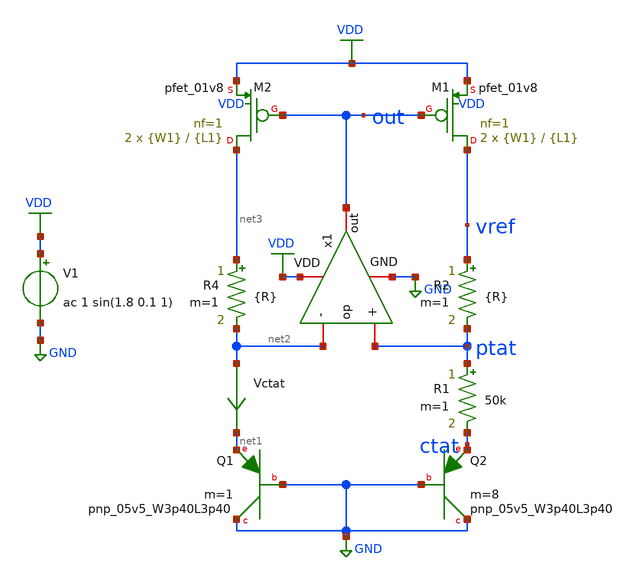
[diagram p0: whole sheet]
** sch_path: xschem/bgr_op3.sch
**.subckt bgr_op3
XQ1 GND GND net1 sky130_fd_pr__pnp_05v5_W3p40L3p40 m=1
XQ2 GND GND ctat sky130_fd_pr__pnp_05v5_W3p40L3p40 m=8
Vctat net2 net1 0
.save i(vctat)
V1 VDD GND ac 1 sin(1.8 0.1 1)
XM1 vref out VDD VDD sky130_fd_pr__pfet_01v8 L={L1} W={W1} nf=1 ad='int((nf+1)/2) * W/nf * 0.29' as='int((nf+2)/2) * W/nf * 0.29'
+ pd='2*int((nf+1)/2) * (W/nf + 0.29)' ps='2*int((nf+2)/2) * (W/nf + 0.29)' nrd='0.29 / W' nrs='0.29 / W'
+ sa=0 sb=0 sd=0 mult=2 m=2
XM2 net3 out VDD VDD sky130_fd_pr__pfet_01v8 L={L1} W={W1} nf=1 ad='int((nf+1)/2) * W/nf * 0.29' as='int((nf+2)/2) * W/nf * 0.29'
+ pd='2*int((nf+1)/2) * (W/nf + 0.29)' ps='2*int((nf+2)/2) * (W/nf + 0.29)' nrd='0.29 / W' nrs='0.29 / W'
+ sa=0 sb=0 sd=0 mult=2 m=2
R1 ptat ctat 50k m=1
R2 vref ptat {R} m=1
R4 net3 net2 {R} m=1
x1 VDD out net2 ptat GND op
**** begin user architecture code


.param L1=0.15
.param W1=1
.param R=489k



** opencircuitdesign pdks install
.lib $::SKYWATER_MODELS/sky130.lib.spice tt




.option savecurrents
.control
save all
op
remzerovec
write bgr_op3.raw
set appendwrite

dc temp -40 85 1
remzerovec
write bgr_op3.raw
*plot (ptat-ctat)
*plot ctat
plot vref

********TC********
meas dc temp_avg_vref avg v(vref)
meas dc temp_vref_27 find v(vref) when temp-sweep=27
meas dc temp_pp_vref PP v(vref)
meas dc temp_vref_max max v(vref)
meas dc temp_max_vref when v(vref)='temp_vref_max'
meas dc temp_vref_min min v(vref)
meas dc temp_min_vref when v(vref)='temp_vref_min'
let vref_tc='((temp_pp_vref*1000000)/(125*temp_avg_vref))'
print vref_tc

******PSRR******
ac dec 1000 1 10Meg
write bgr_op3.raw
remzerovec
plot vdb(vref)
meas ac psrr find vdb(vref) at=1k

****Power****
tran 0.1 0.2
write bgr_op3.raw
remzerovec
meas tran ave_v avg vdd
meas tran ave_i avg i(v1)
let ave_power='ave_v*(-ave_i)
*plot vdd vref
*plot -i(v1)
print ave_power

*******LS******
dc v1 0 3.5 0.1
write bgr_op3.raw
remzerovec
meas dc vref_max max v(vref) from=1.62 to=1.98
meas dc vref_min min v(vref) from=1.62 to=1.98
let ls='(vref_max-vref_min)/(1.98-1.62)'
print ls

.endc


**** end user architecture code
**.ends

* expanding   symbol:  op.sym # of pins=5
** sym_path: xschem/op.sym
** sch_path: xschem/op.sch
.subckt op VDD out - + GND
*.iopin VDD
*.iopin GND
*.iopin -
*.iopin +
*.iopin out
**** begin user architecture code


.param L=2.7
.param W=1.5


**** end user architecture code
XM1 net1 net2 VDD VDD sky130_fd_pr__pfet_01v8_lvt L={L} W={W} nf=1 ad='int((nf+1)/2) * W/nf * 0.29' as='int((nf+2)/2)
+ * W/nf * 0.29' pd='2*int((nf+1)/2) * (W/nf + 0.29)' ps='2*int((nf+2)/2) * (W/nf + 0.29)' nrd='0.29 /
+ W' nrs='0.29 / W' sa=0 sb=0 sd=0 mult=4 m=4
XM2 net2 net2 VDD VDD sky130_fd_pr__pfet_01v8_lvt L={L} W={W} nf=1 ad='int((nf+1)/2) * W/nf * 0.29' as='int((nf+2)/2)
+ * W/nf * 0.29' pd='2*int((nf+1)/2) * (W/nf + 0.29)' ps='2*int((nf+2)/2) * (W/nf + 0.29)' nrd='0.29 /
+ W' nrs='0.29 / W' sa=0 sb=0 sd=0 mult=4 m=4
XM3 net1 + net3 GND sky130_fd_pr__nfet_01v8_lvt L={L} W={W} nf=1 ad='int((nf+1)/2) * W/nf * 0.29' as='int((nf+2)/2)
+ * W/nf * 0.29' pd='2*int((nf+1)/2) * (W/nf + 0.29)' ps='2*int((nf+2)/2) * (W/nf + 0.29)' nrd='0.29 /
+ W' nrs='0.29 / W' sa=0 sb=0 sd=0 mult=4 m=4
XM4 net2 - net3 GND sky130_fd_pr__nfet_01v8_lvt L={L} W={W} nf=1 ad='int((nf+1)/2) * W/nf * 0.29' as='int((nf+2)/2)
+ * W/nf * 0.29' pd='2*int((nf+1)/2) * (W/nf + 0.29)' ps='2*int((nf+2)/2) * (W/nf + 0.29)' nrd='0.29 /
+ W' nrs='0.29 / W' sa=0 sb=0 sd=0 mult=4 m=4
XM5 net3 bias GND GND sky130_fd_pr__nfet_01v8_lvt L={L} W={W} nf=1 ad='int((nf+1)/2) * W/nf * 0.29' as='int((nf+2)/2)
+ * W/nf * 0.29' pd='2*int((nf+1)/2) * (W/nf + 0.29)' ps='2*int((nf+2)/2) * (W/nf + 0.29)' nrd='0.29 /
+ W' nrs='0.29 / W' sa=0 sb=0 sd=0 mult=4 m=4
XM6 bias net4 VDD VDD sky130_fd_pr__pfet_01v8_lvt L={L*2} W={W/2} nf=1 ad='int((nf+1)/2) * W/nf * 0.29' as='int((nf+2)/2)
+ * W/nf * 0.29' pd='2*int((nf+1)/2) * (W/nf + 0.29)' ps='2*int((nf+2)/2) * (W/nf + 0.29)' nrd='0.29 /
+ W' nrs='0.29 / W' sa=0 sb=0 sd=0 mult=4 m=4
XM7 net4 net4 VDD VDD sky130_fd_pr__pfet_01v8_lvt L={L*2} W={W/2} nf=1 ad='int((nf+1)/2) * W/nf * 0.29' as='int((nf+2)/2)
+ * W/nf * 0.29' pd='2*int((nf+1)/2) * (W/nf + 0.29)' ps='2*int((nf+2)/2) * (W/nf + 0.29)' nrd='0.29 /
+ W' nrs='0.29 / W' sa=0 sb=0 sd=0 mult=4 m=4
XM8 net4 bias GND GND sky130_fd_pr__nfet_01v8_lvt L={L*2} W={W/2} nf=1 ad='int((nf+1)/2) * W/nf * 0.29' as='int((nf+2)/2)
+ * W/nf * 0.29' pd='2*int((nf+1)/2) * (W/nf + 0.29)' ps='2*int((nf+2)/2) * (W/nf + 0.29)' nrd='0.29 /
+ W' nrs='0.29 / W' sa=0 sb=0 sd=0 mult=4 m=4
XM9 bias bias GND GND sky130_fd_pr__nfet_01v8_lvt L={L*2} W={W/2} nf=1 ad='int((nf+1)/2) * W/nf * 0.29' as='int((nf+2)/2)
+ * W/nf * 0.29' pd='2*int((nf+1)/2) * (W/nf + 0.29)' ps='2*int((nf+2)/2) * (W/nf + 0.29)' nrd='0.29 /
+ W' nrs='0.29 / W' sa=0 sb=0 sd=0 mult=4 m=4
XM10 out bias GND GND sky130_fd_pr__nfet_01v8_lvt L={L} W={W/2} nf=1 ad='int((nf+1)/2) * W/nf * 0.29' as='int((nf+2)/2)
+ * W/nf * 0.29' pd='2*int((nf+1)/2) * (W/nf + 0.29)' ps='2*int((nf+2)/2) * (W/nf + 0.29)' nrd='0.29 /
+ W' nrs='0.29 / W' sa=0 sb=0 sd=0 mult=4 m=4
XM11 out net1 VDD VDD sky130_fd_pr__pfet_01v8_lvt L={L} W={W} nf=1 ad='int((nf+1)/2) * W/nf * 0.29' as='int((nf+2)/2)
+ * W/nf * 0.29' pd='2*int((nf+1)/2) * (W/nf + 0.29)' ps='2*int((nf+2)/2) * (W/nf + 0.29)' nrd='0.29 /
+ W' nrs='0.29 / W' sa=0 sb=0 sd=0 mult=4 m=4
C2 out net5 1p m=1
R2 net5 net1 40k m=1
.ends

.GLOBAL VDD
.GLOBAL GND
.end
